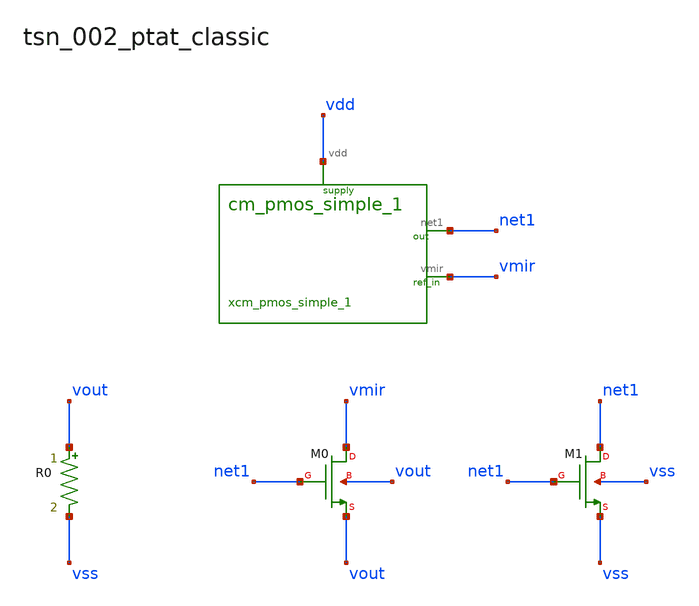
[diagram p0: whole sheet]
** sch_path: analog-db/raw/tsn_002_ptat_classic/hier/tsn_002_ptat_classic.sch
**.subckt tsn_002_ptat_classic
xcm_pmos_simple_1 net1 vmir vdd cm_pmos_simple_1
R0 vout vss x_r0 m=1
XM0 vmir net1 vout vout sg13_lv_nmos w=x_dut_xm0_w l=x_dut_xm0_l ng=1 m=x_dut_xm0_m
XM1 net1 net1 vss vss sg13_lv_nmos w=x_dut_xm1_w l=x_dut_xm1_l ng=1 m=x_dut_xm1_m
**.ends

* expanding   symbol:  blocks/cm_pmos_simple_1.sym # of pins=3
** sym_path: analog-db/raw/tsn_002_ptat_classic/hier/blocks/cm_pmos_simple_1.sym
** sch_path: analog-db/raw/tsn_002_ptat_classic/hier/blocks/cm_pmos_simple_1.sch
.subckt cm_pmos_simple_1 net1 vmir vdd
*.iopin vdd
*.opin vmir
*.opin net1
XM3 vmir vmir vdd vdd sg13_lv_pmos w=x_dut_xm3_w l=x_dut_xm3_l ng=1 m=x_dut_xm3_m
XM4 net1 vmir vdd vdd sg13_lv_pmos w=x_dut_xm4_w l=x_dut_xm4_l ng=1 m=x_dut_xm4_m
.ends

.end
